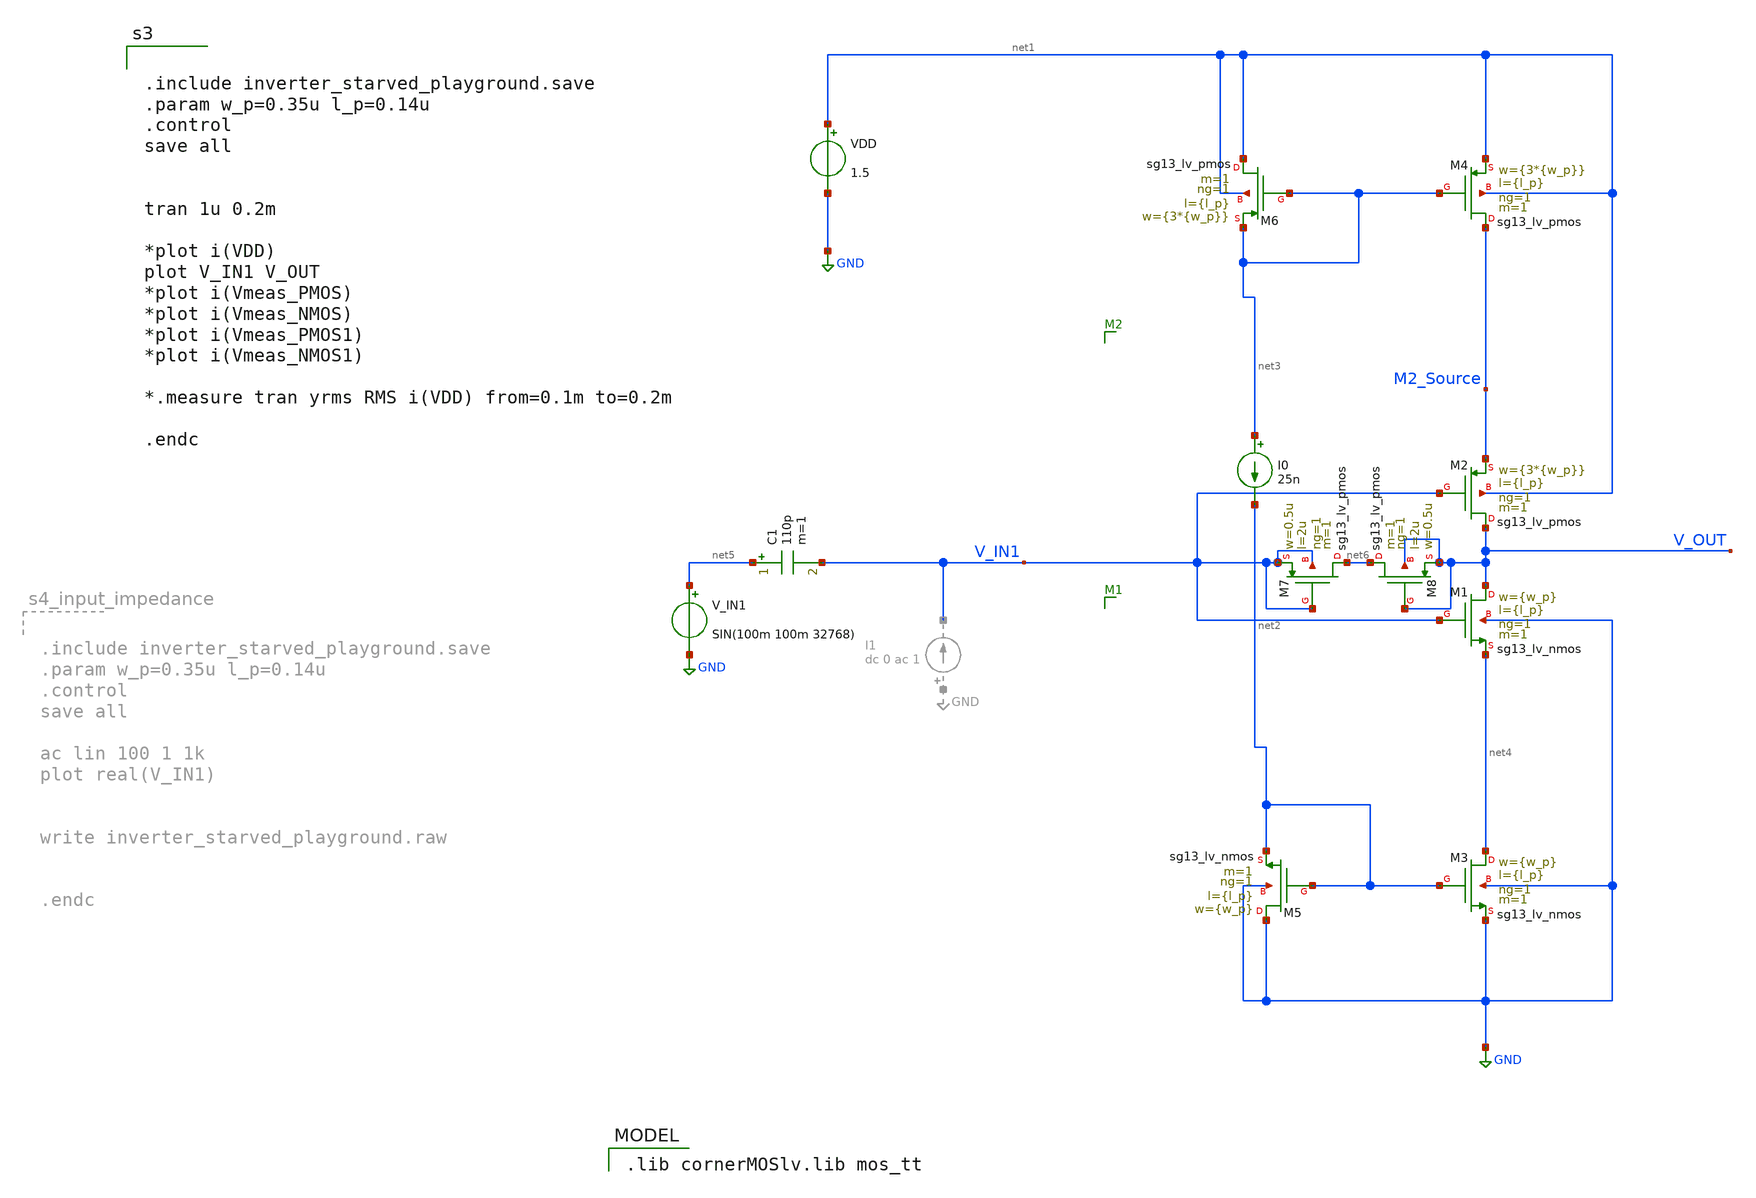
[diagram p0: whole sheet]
** sch_path: inverter_starved_playground.sch
**.subckt inverter_starved_playground
XM1 V_OUT V_IN1 net4 GND sg13_lv_nmos w={w_p} l={l_p} ng=1 m=1 mm_ok=1
XM2 V_OUT V_IN1 M2_Source net1 sg13_lv_pmos w={3*{w_p}} l={l_p} ng=1 m=1 mm_ok=1
VDD net1 GND 1.5
XM3 net4 net2 GND GND sg13_lv_nmos w={w_p} l={l_p} ng=1 m=1 mm_ok=1
XM4 M2_Source net3 net1 net1 sg13_lv_pmos w={3*{w_p}} l={l_p} ng=1 m=1 mm_ok=1
XM5 GND net2 net2 GND sg13_lv_nmos w={w_p} l={l_p} ng=1 m=1 mm_ok=1
XM6 net1 net3 net3 net1 sg13_lv_pmos w={3*{w_p}} l={l_p} ng=1 m=1 mm_ok=1
I0 net3 net2 25n
V_IN1 net5 GND SIN(100m 100m 32768)
C1 net5 V_IN1 110p m=1
XM7 net6 V_IN1 V_IN1 V_IN1 sg13_lv_pmos w=0.5u l=2u ng=1 m=1 mm_ok=1
XM8 net6 V_OUT V_OUT V_OUT sg13_lv_pmos w=0.5u l=2u ng=1 m=1 mm_ok=1
**** begin user architecture code
 .lib cornerMOSlv.lib mos_tt



.include inverter_starved_playground.save
.param w_p=0.35u l_p=0.14u
.control
save all


tran 1u 0.2m

*plot i(VDD)
plot V_IN1 V_OUT
*plot i(Vmeas_PMOS)
*plot i(Vmeas_NMOS)
*plot i(Vmeas_PMOS1)
*plot i(Vmeas_NMOS1)

*.measure tran yrms RMS i(VDD) from=0.1m to=0.2m

.endc


**** end user architecture code
**.ends
.GLOBAL GND
.end
